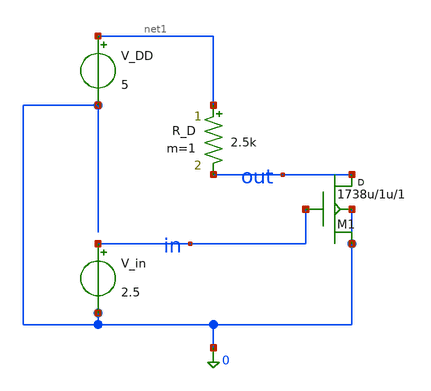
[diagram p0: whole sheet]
** sch_path: nmos_cs_amplifier.sch
**.subckt nmos_cs_amplifier
V_DD net1 0 5
R_D net1 out 2.5k m=1
M1 out in 0 0 ALD1101 w=1738u l=1u m=1
V_in in 0 2.5
**** begin user architecture code

.MODEL ALD1101 NMOS LEVEL = 2 UO = 12.72 VTO = 0.6766 NFS = 1.154E12 TOX = 1E-08 NSUB = 3.892E17
+ UCRIT = 4.582E05 UEXP = 0.07025 VMAX = 6363 RS = 9.491 RD = 5.659 XJ = 4.787E-09 LD = 0 DELTA = 1E-12
+ NEFF = 0.8345 NSS = -3.801 CGSO = 1.15E-9 CGDO = 1.15E-9 CGBO = 0 CBD = 0 CBS = 0 CJ = 0 MJ = 0.5  CJSW
+ = 0 MJSW = 0.6057 IS = 1.0E-14 PB = 0.8 FC = 0.5 NEFF=5



.dc V_in 0 5 0.01




.tran 10u 2m


**** end user architecture code
**.ends
.end
